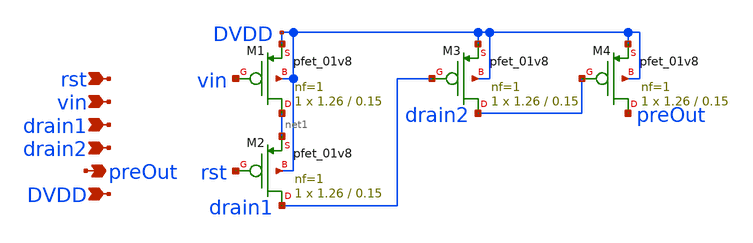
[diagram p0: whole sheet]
** sch_path: xschem/pcell_pfd.sch
**.subckt pcell_pfd rst vin drain1 drain2 preOut DVDD
*.ipin rst
*.ipin vin
*.ipin drain1
*.ipin drain2
*.opin preOut
*.ipin DVDD
XM1 net1 vin DVDD DVDD sky130_fd_pr__pfet_01v8 L=0.15 W=1.26 nf=1 ad='int((nf+1)/2) * W/nf * 0.29' as='int((nf+2)/2) * W/nf * 0.29'
+ pd='2*int((nf+1)/2) * (W/nf + 0.29)' ps='2*int((nf+2)/2) * (W/nf + 0.29)' nrd='0.29 / W' nrs='0.29 / W'
+ sa=0 sb=0 sd=0 mult=1 m=1
XM2 drain1 rst net1 DVDD sky130_fd_pr__pfet_01v8 L=0.15 W=1.26 nf=1 ad='int((nf+1)/2) * W/nf * 0.29'
+ as='int((nf+2)/2) * W/nf * 0.29' pd='2*int((nf+1)/2) * (W/nf + 0.29)' ps='2*int((nf+2)/2) * (W/nf + 0.29)'
+ nrd='0.29 / W' nrs='0.29 / W' sa=0 sb=0 sd=0 mult=1 m=1
XM3 drain2 drain1 DVDD DVDD sky130_fd_pr__pfet_01v8 L=0.15 W=1.26 nf=1 ad='int((nf+1)/2) * W/nf * 0.29'
+ as='int((nf+2)/2) * W/nf * 0.29' pd='2*int((nf+1)/2) * (W/nf + 0.29)' ps='2*int((nf+2)/2) * (W/nf + 0.29)'
+ nrd='0.29 / W' nrs='0.29 / W' sa=0 sb=0 sd=0 mult=1 m=1
XM4 preOut drain2 DVDD DVDD sky130_fd_pr__pfet_01v8 L=0.15 W=1.26 nf=1 ad='int((nf+1)/2) * W/nf * 0.29'
+ as='int((nf+2)/2) * W/nf * 0.29' pd='2*int((nf+1)/2) * (W/nf + 0.29)' ps='2*int((nf+2)/2) * (W/nf + 0.29)'
+ nrd='0.29 / W' nrs='0.29 / W' sa=0 sb=0 sd=0 mult=1 m=1
**.ends
.end
